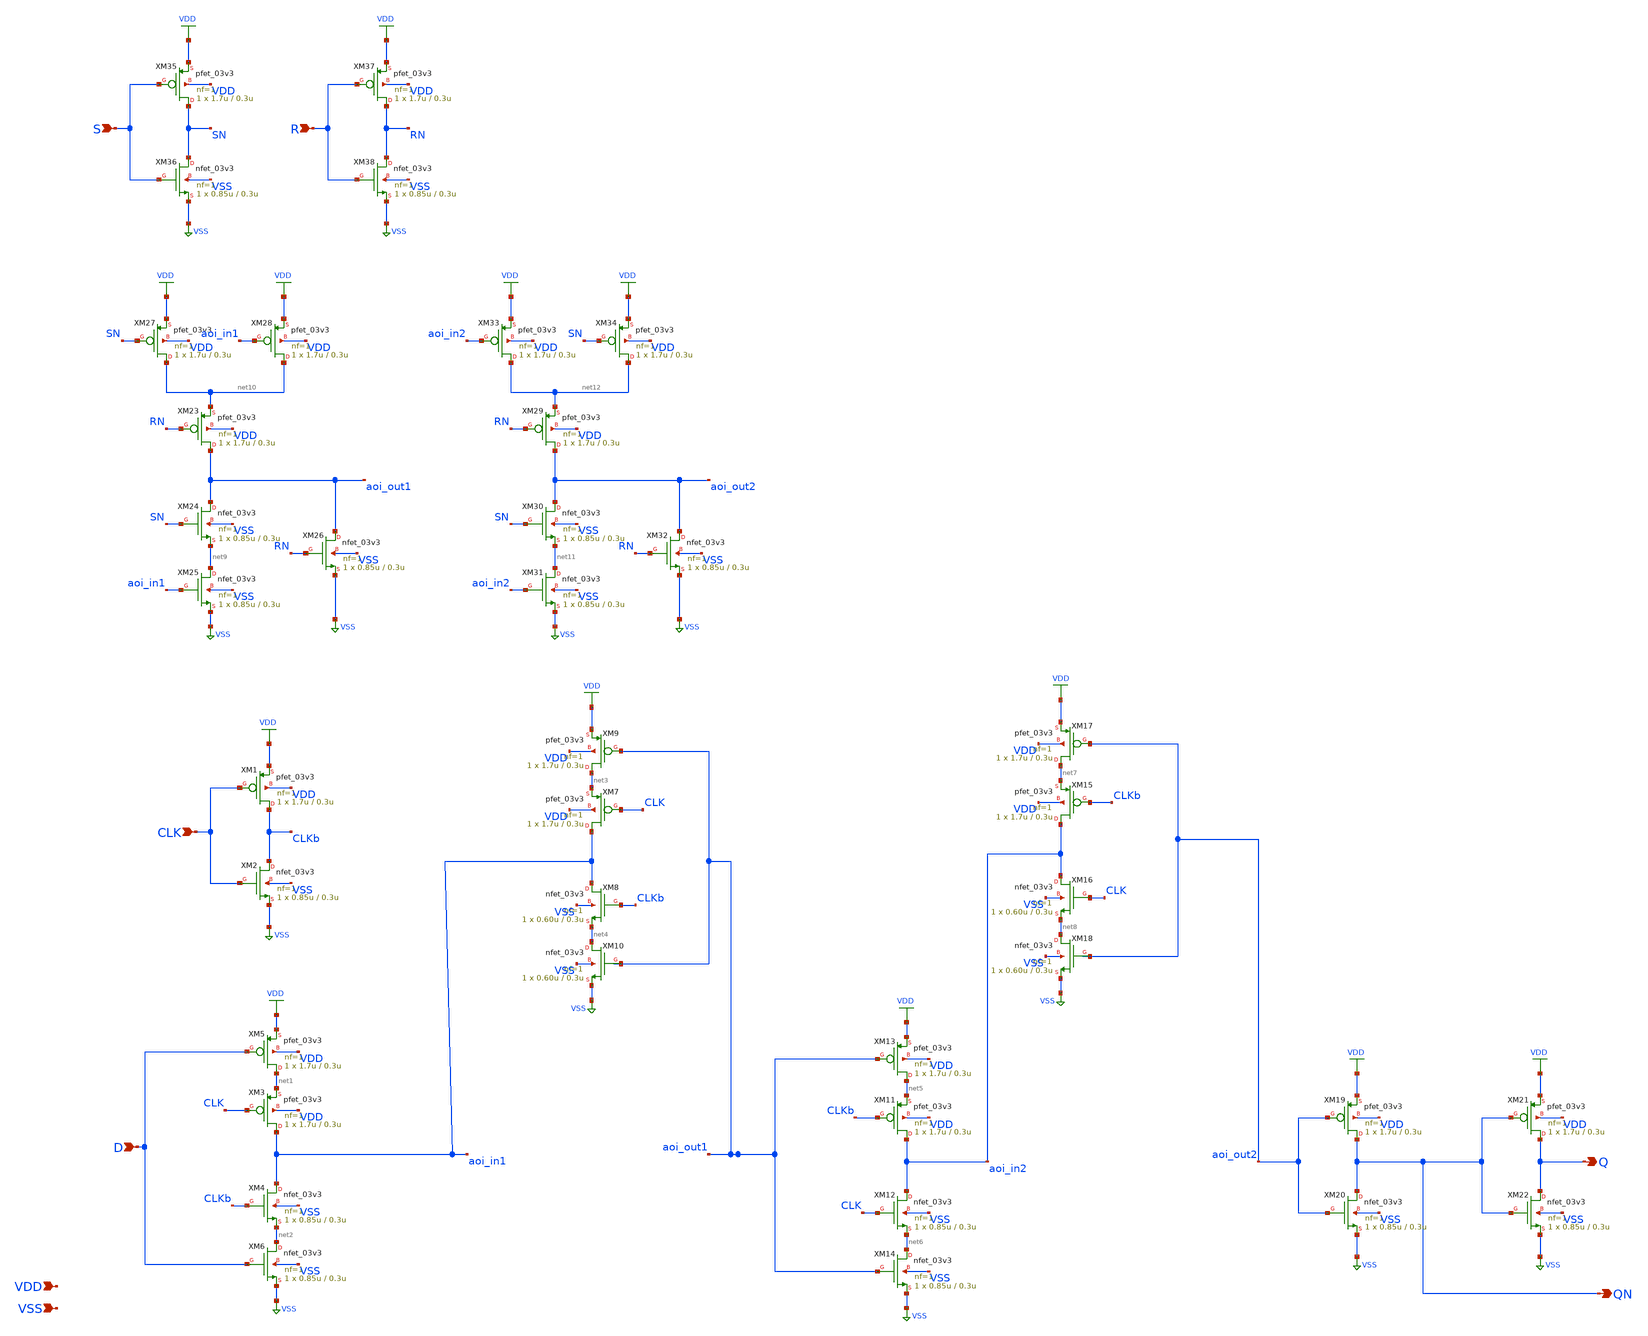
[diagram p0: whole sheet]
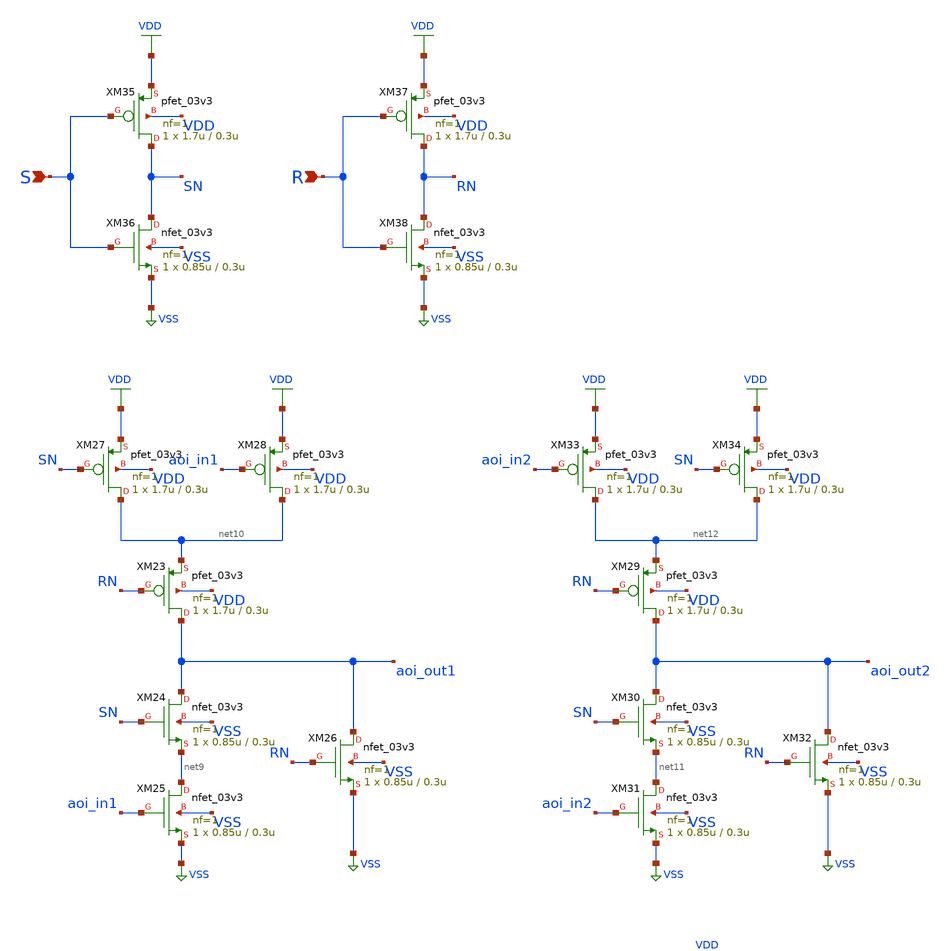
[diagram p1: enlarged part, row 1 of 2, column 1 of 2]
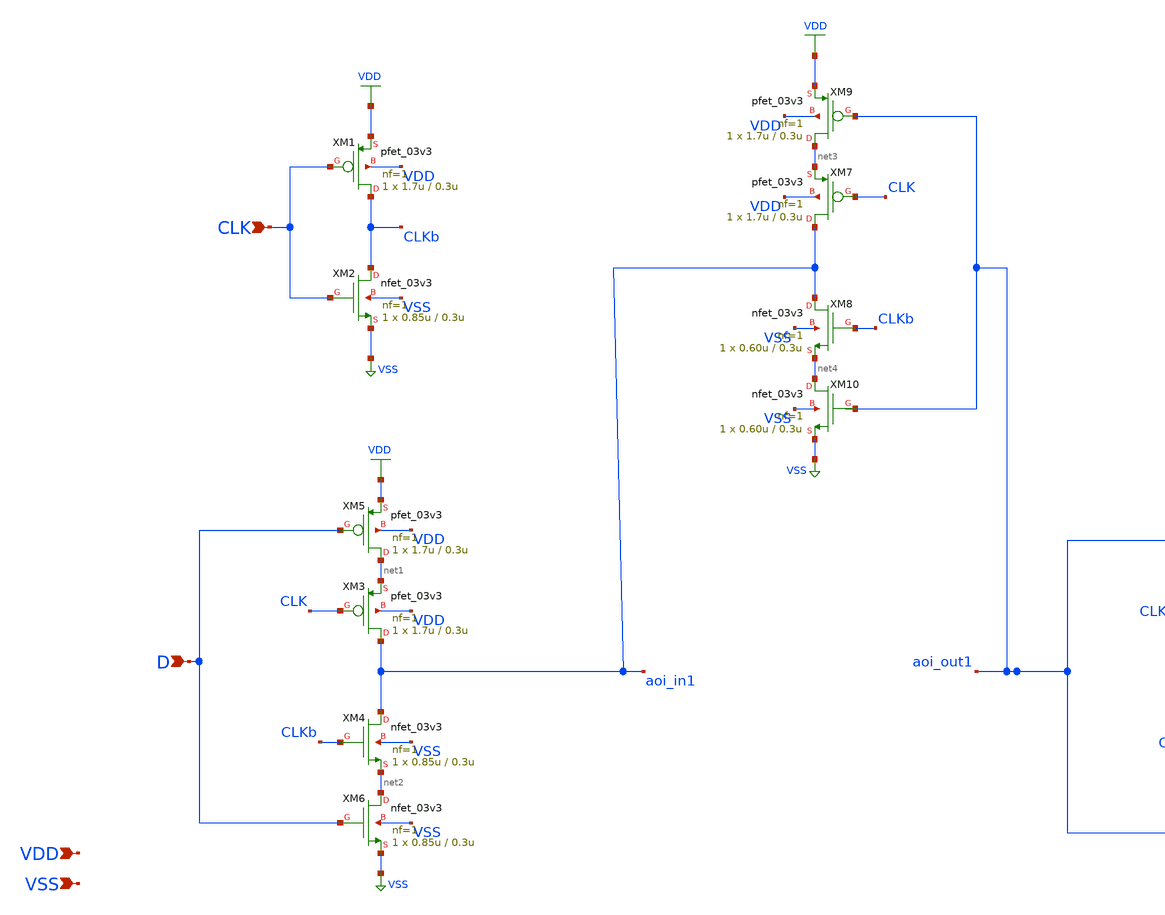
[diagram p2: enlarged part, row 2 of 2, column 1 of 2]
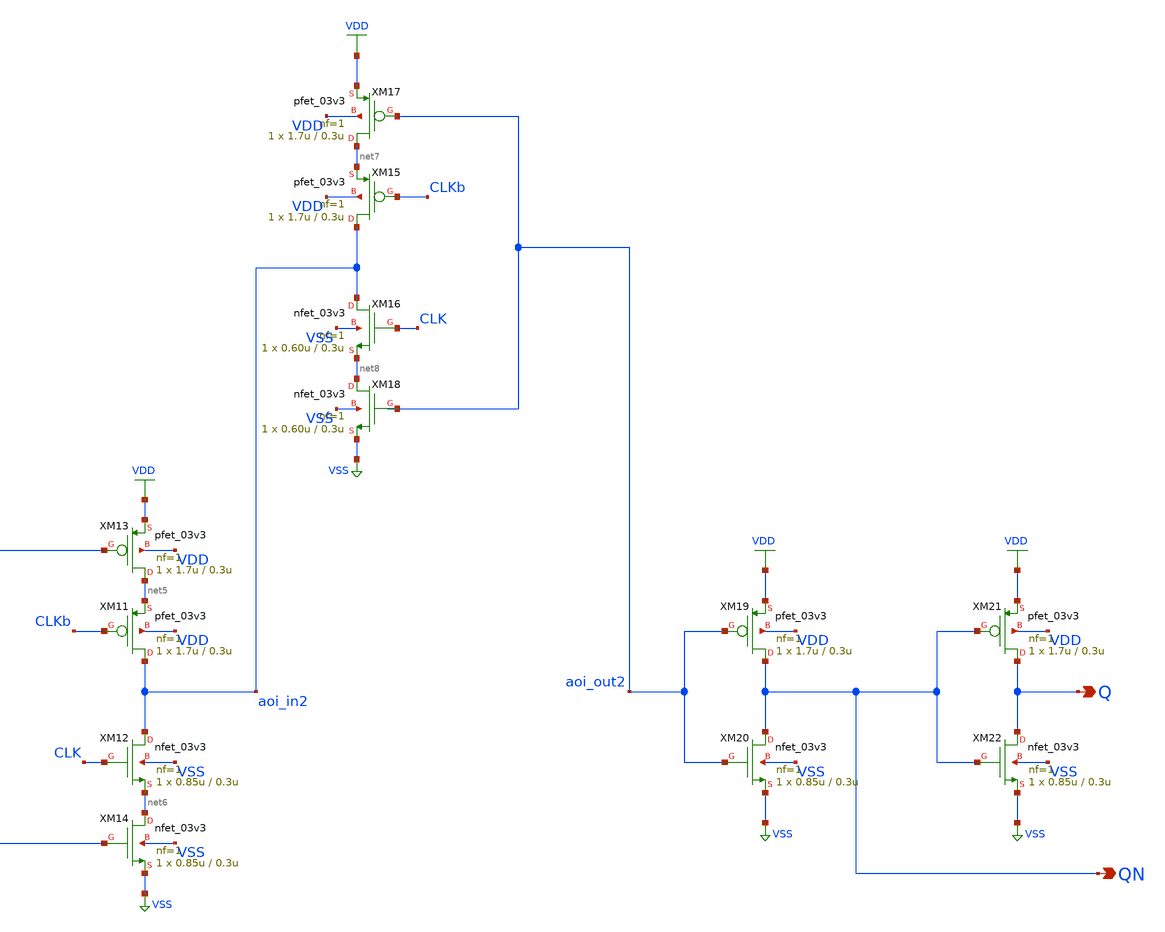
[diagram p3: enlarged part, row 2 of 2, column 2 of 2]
** sch_path: gf180mcu_osu_sc_gp9t3v3/xschem/gf180mcu_osu_sc_gp9t3v3__dffsr_1.sch
**.subckt gf180mcu_osu_sc_gp9t3v3__dffsr_1 D CLK Q QN S R VDD VSS
*.ipin D
*.ipin CLK
*.opin Q
*.opin QN
*.ipin S
*.ipin R
*.ipin VDD
*.ipin VSS
XM1 CLKb CLK VDD VDD pfet_03v3 L=0.3u W=1.7u nf=1 ad='int((nf+1)/2) * W/nf * 0.18u' as='int((nf+2)/2) * W/nf * 0.18u'
+ pd='2*int((nf+1)/2) * (W/nf + 0.18u)' ps='2*int((nf+2)/2) * (W/nf + 0.18u)' nrd='0.18u / W' nrs='0.18u / W'
+ sa=0 sb=0 sd=0 m=1
XM2 CLKb CLK VSS VSS nfet_03v3 L=0.3u W=0.85u nf=1 ad='int((nf+1)/2) * W/nf * 0.18u' as='int((nf+2)/2) * W/nf * 0.18u'
+ pd='2*int((nf+1)/2) * (W/nf + 0.18u)' ps='2*int((nf+2)/2) * (W/nf + 0.18u)' nrd='0.18u / W' nrs='0.18u / W'
+ sa=0 sb=0 sd=0 m=1
XM3 aoi_in1 CLK net1 VDD pfet_03v3 L=0.3u W=1.7u nf=1 ad='int((nf+1)/2) * W/nf * 0.18u' as='int((nf+2)/2) * W/nf * 0.18u'
+ pd='2*int((nf+1)/2) * (W/nf + 0.18u)' ps='2*int((nf+2)/2) * (W/nf + 0.18u)' nrd='0.18u / W' nrs='0.18u / W'
+ sa=0 sb=0 sd=0 m=1
XM4 aoi_in1 CLKb net2 VSS nfet_03v3 L=0.3u W=0.85u nf=1 ad='int((nf+1)/2) * W/nf * 0.18u' as='int((nf+2)/2) * W/nf * 0.18u'
+ pd='2*int((nf+1)/2) * (W/nf + 0.18u)' ps='2*int((nf+2)/2) * (W/nf + 0.18u)' nrd='0.18u / W' nrs='0.18u / W'
+ sa=0 sb=0 sd=0 m=1
XM5 net1 D VDD VDD pfet_03v3 L=0.3u W=1.7u nf=1 ad='int((nf+1)/2) * W/nf * 0.18u' as='int((nf+2)/2) * W/nf * 0.18u'
+ pd='2*int((nf+1)/2) * (W/nf + 0.18u)' ps='2*int((nf+2)/2) * (W/nf + 0.18u)' nrd='0.18u / W' nrs='0.18u / W'
+ sa=0 sb=0 sd=0 m=1
XM6 net2 D VSS VSS nfet_03v3 L=0.3u W=0.85u nf=1 ad='int((nf+1)/2) * W/nf * 0.18u' as='int((nf+2)/2) * W/nf * 0.18u'
+ pd='2*int((nf+1)/2) * (W/nf + 0.18u)' ps='2*int((nf+2)/2) * (W/nf + 0.18u)' nrd='0.18u / W' nrs='0.18u / W'
+ sa=0 sb=0 sd=0 m=1
XM7 aoi_in1 CLK net3 VDD pfet_03v3 L=0.3u W=1.7u nf=1 ad='int((nf+1)/2) * W/nf * 0.18u' as='int((nf+2)/2) * W/nf * 0.18u'
+ pd='2*int((nf+1)/2) * (W/nf + 0.18u)' ps='2*int((nf+2)/2) * (W/nf + 0.18u)' nrd='0.18u / W' nrs='0.18u / W'
+ sa=0 sb=0 sd=0 m=1
XM8 aoi_in1 CLKb net4 VSS nfet_03v3 L=0.3u W=0.60u nf=1 ad='int((nf+1)/2) * W/nf * 0.18u' as='int((nf+2)/2) * W/nf * 0.18u'
+ pd='2*int((nf+1)/2) * (W/nf + 0.18u)' ps='2*int((nf+2)/2) * (W/nf + 0.18u)' nrd='0.18u / W' nrs='0.18u / W'
+ sa=0 sb=0 sd=0 m=1
XM9 net3 aoi_out1 VDD VDD pfet_03v3 L=0.3u W=1.7u nf=1 ad='int((nf+1)/2) * W/nf * 0.18u' as='int((nf+2)/2) * W/nf * 0.18u'
+ pd='2*int((nf+1)/2) * (W/nf + 0.18u)' ps='2*int((nf+2)/2) * (W/nf + 0.18u)' nrd='0.18u / W' nrs='0.18u / W'
+ sa=0 sb=0 sd=0 m=1
XM10 net4 aoi_out1 VSS VSS nfet_03v3 L=0.3u W=0.60u nf=1 ad='int((nf+1)/2) * W/nf * 0.18u' as='int((nf+2)/2) * W/nf * 0.18u'
+ pd='2*int((nf+1)/2) * (W/nf + 0.18u)' ps='2*int((nf+2)/2) * (W/nf + 0.18u)' nrd='0.18u / W' nrs='0.18u / W'
+ sa=0 sb=0 sd=0 m=1
XM11 aoi_in2 CLKb net5 VDD pfet_03v3 L=0.3u W=1.7u nf=1 ad='int((nf+1)/2) * W/nf * 0.18u' as='int((nf+2)/2) * W/nf * 0.18u'
+ pd='2*int((nf+1)/2) * (W/nf + 0.18u)' ps='2*int((nf+2)/2) * (W/nf + 0.18u)' nrd='0.18u / W' nrs='0.18u / W'
+ sa=0 sb=0 sd=0 m=1
XM12 aoi_in2 CLK net6 VSS nfet_03v3 L=0.3u W=0.85u nf=1 ad='int((nf+1)/2) * W/nf * 0.18u' as='int((nf+2)/2) * W/nf * 0.18u'
+ pd='2*int((nf+1)/2) * (W/nf + 0.18u)' ps='2*int((nf+2)/2) * (W/nf + 0.18u)' nrd='0.18u / W' nrs='0.18u / W'
+ sa=0 sb=0 sd=0 m=1
XM13 net5 aoi_out1 VDD VDD pfet_03v3 L=0.3u W=1.7u nf=1 ad='int((nf+1)/2) * W/nf * 0.18u' as='int((nf+2)/2) * W/nf * 0.18u'
+ pd='2*int((nf+1)/2) * (W/nf + 0.18u)' ps='2*int((nf+2)/2) * (W/nf + 0.18u)' nrd='0.18u / W' nrs='0.18u / W'
+ sa=0 sb=0 sd=0 m=1
XM14 net6 aoi_out1 VSS VSS nfet_03v3 L=0.3u W=0.85u nf=1 ad='int((nf+1)/2) * W/nf * 0.18u' as='int((nf+2)/2) * W/nf * 0.18u'
+ pd='2*int((nf+1)/2) * (W/nf + 0.18u)' ps='2*int((nf+2)/2) * (W/nf + 0.18u)' nrd='0.18u / W' nrs='0.18u / W'
+ sa=0 sb=0 sd=0 m=1
XM15 aoi_in2 CLKb net7 VDD pfet_03v3 L=0.3u W=1.7u nf=1 ad='int((nf+1)/2) * W/nf * 0.18u' as='int((nf+2)/2) * W/nf * 0.18u'
+ pd='2*int((nf+1)/2) * (W/nf + 0.18u)' ps='2*int((nf+2)/2) * (W/nf + 0.18u)' nrd='0.18u / W' nrs='0.18u / W'
+ sa=0 sb=0 sd=0 m=1
XM16 aoi_in2 CLK net8 VSS nfet_03v3 L=0.3u W=0.60u nf=1 ad='int((nf+1)/2) * W/nf * 0.18u' as='int((nf+2)/2) * W/nf * 0.18u'
+ pd='2*int((nf+1)/2) * (W/nf + 0.18u)' ps='2*int((nf+2)/2) * (W/nf + 0.18u)' nrd='0.18u / W' nrs='0.18u / W'
+ sa=0 sb=0 sd=0 m=1
XM17 net7 aoi_out2 VDD VDD pfet_03v3 L=0.3u W=1.7u nf=1 ad='int((nf+1)/2) * W/nf * 0.18u' as='int((nf+2)/2) * W/nf * 0.18u'
+ pd='2*int((nf+1)/2) * (W/nf + 0.18u)' ps='2*int((nf+2)/2) * (W/nf + 0.18u)' nrd='0.18u / W' nrs='0.18u / W'
+ sa=0 sb=0 sd=0 m=1
XM18 net8 aoi_out2 VSS VSS nfet_03v3 L=0.3u W=0.60u nf=1 ad='int((nf+1)/2) * W/nf * 0.18u' as='int((nf+2)/2) * W/nf * 0.18u'
+ pd='2*int((nf+1)/2) * (W/nf + 0.18u)' ps='2*int((nf+2)/2) * (W/nf + 0.18u)' nrd='0.18u / W' nrs='0.18u / W'
+ sa=0 sb=0 sd=0 m=1
XM19 QN aoi_out2 VDD VDD pfet_03v3 L=0.3u W=1.7u nf=1 ad='int((nf+1)/2) * W/nf * 0.18u' as='int((nf+2)/2) * W/nf * 0.18u'
+ pd='2*int((nf+1)/2) * (W/nf + 0.18u)' ps='2*int((nf+2)/2) * (W/nf + 0.18u)' nrd='0.18u / W' nrs='0.18u / W'
+ sa=0 sb=0 sd=0 m=1
XM20 QN aoi_out2 VSS VSS nfet_03v3 L=0.3u W=0.85u nf=1 ad='int((nf+1)/2) * W/nf * 0.18u' as='int((nf+2)/2) * W/nf * 0.18u'
+ pd='2*int((nf+1)/2) * (W/nf + 0.18u)' ps='2*int((nf+2)/2) * (W/nf + 0.18u)' nrd='0.18u / W' nrs='0.18u / W'
+ sa=0 sb=0 sd=0 m=1
XM21 Q QN VDD VDD pfet_03v3 L=0.3u W=1.7u nf=1 ad='int((nf+1)/2) * W/nf * 0.18u' as='int((nf+2)/2) * W/nf * 0.18u'
+ pd='2*int((nf+1)/2) * (W/nf + 0.18u)' ps='2*int((nf+2)/2) * (W/nf + 0.18u)' nrd='0.18u / W' nrs='0.18u / W'
+ sa=0 sb=0 sd=0 m=1
XM22 Q QN VSS VSS nfet_03v3 L=0.3u W=0.85u nf=1 ad='int((nf+1)/2) * W/nf * 0.18u' as='int((nf+2)/2) * W/nf * 0.18u'
+ pd='2*int((nf+1)/2) * (W/nf + 0.18u)' ps='2*int((nf+2)/2) * (W/nf + 0.18u)' nrd='0.18u / W' nrs='0.18u / W'
+ sa=0 sb=0 sd=0 m=1
XM23 aoi_out1 RN net10 VDD pfet_03v3 L=0.3u W=1.7u nf=1 ad='int((nf+1)/2) * W/nf * 0.18u' as='int((nf+2)/2) * W/nf * 0.18u'
+ pd='2*int((nf+1)/2) * (W/nf + 0.18u)' ps='2*int((nf+2)/2) * (W/nf + 0.18u)' nrd='0.18u / W' nrs='0.18u / W'
+ sa=0 sb=0 sd=0 m=1
XM24 aoi_out1 SN net9 VSS nfet_03v3 L=0.3u W=0.85u nf=1 ad='int((nf+1)/2) * W/nf * 0.18u' as='int((nf+2)/2) * W/nf * 0.18u'
+ pd='2*int((nf+1)/2) * (W/nf + 0.18u)' ps='2*int((nf+2)/2) * (W/nf + 0.18u)' nrd='0.18u / W' nrs='0.18u / W'
+ sa=0 sb=0 sd=0 m=1
XM25 net9 aoi_in1 VSS VSS nfet_03v3 L=0.3u W=0.85u nf=1 ad='int((nf+1)/2) * W/nf * 0.18u' as='int((nf+2)/2) * W/nf * 0.18u'
+ pd='2*int((nf+1)/2) * (W/nf + 0.18u)' ps='2*int((nf+2)/2) * (W/nf + 0.18u)' nrd='0.18u / W' nrs='0.18u / W'
+ sa=0 sb=0 sd=0 m=1
XM26 aoi_out1 RN VSS VSS nfet_03v3 L=0.3u W=0.85u nf=1 ad='int((nf+1)/2) * W/nf * 0.18u' as='int((nf+2)/2) * W/nf * 0.18u'
+ pd='2*int((nf+1)/2) * (W/nf + 0.18u)' ps='2*int((nf+2)/2) * (W/nf + 0.18u)' nrd='0.18u / W' nrs='0.18u / W'
+ sa=0 sb=0 sd=0 m=1
XM27 net10 SN VDD VDD pfet_03v3 L=0.3u W=1.7u nf=1 ad='int((nf+1)/2) * W/nf * 0.18u' as='int((nf+2)/2) * W/nf * 0.18u'
+ pd='2*int((nf+1)/2) * (W/nf + 0.18u)' ps='2*int((nf+2)/2) * (W/nf + 0.18u)' nrd='0.18u / W' nrs='0.18u / W'
+ sa=0 sb=0 sd=0 m=1
XM28 net10 aoi_in1 VDD VDD pfet_03v3 L=0.3u W=1.7u nf=1 ad='int((nf+1)/2) * W/nf * 0.18u' as='int((nf+2)/2) * W/nf * 0.18u'
+ pd='2*int((nf+1)/2) * (W/nf + 0.18u)' ps='2*int((nf+2)/2) * (W/nf + 0.18u)' nrd='0.18u / W' nrs='0.18u / W'
+ sa=0 sb=0 sd=0 m=1
XM29 aoi_out2 RN net12 VDD pfet_03v3 L=0.3u W=1.7u nf=1 ad='int((nf+1)/2) * W/nf * 0.18u' as='int((nf+2)/2) * W/nf * 0.18u'
+ pd='2*int((nf+1)/2) * (W/nf + 0.18u)' ps='2*int((nf+2)/2) * (W/nf + 0.18u)' nrd='0.18u / W' nrs='0.18u / W'
+ sa=0 sb=0 sd=0 m=1
XM30 aoi_out2 SN net11 VSS nfet_03v3 L=0.3u W=0.85u nf=1 ad='int((nf+1)/2) * W/nf * 0.18u' as='int((nf+2)/2) * W/nf * 0.18u'
+ pd='2*int((nf+1)/2) * (W/nf + 0.18u)' ps='2*int((nf+2)/2) * (W/nf + 0.18u)' nrd='0.18u / W' nrs='0.18u / W'
+ sa=0 sb=0 sd=0 m=1
XM31 net11 aoi_in2 VSS VSS nfet_03v3 L=0.3u W=0.85u nf=1 ad='int((nf+1)/2) * W/nf * 0.18u' as='int((nf+2)/2) * W/nf * 0.18u'
+ pd='2*int((nf+1)/2) * (W/nf + 0.18u)' ps='2*int((nf+2)/2) * (W/nf + 0.18u)' nrd='0.18u / W' nrs='0.18u / W'
+ sa=0 sb=0 sd=0 m=1
XM32 aoi_out2 RN VSS VSS nfet_03v3 L=0.3u W=0.85u nf=1 ad='int((nf+1)/2) * W/nf * 0.18u' as='int((nf+2)/2) * W/nf * 0.18u'
+ pd='2*int((nf+1)/2) * (W/nf + 0.18u)' ps='2*int((nf+2)/2) * (W/nf + 0.18u)' nrd='0.18u / W' nrs='0.18u / W'
+ sa=0 sb=0 sd=0 m=1
XM33 net12 aoi_in2 VDD VDD pfet_03v3 L=0.3u W=1.7u nf=1 ad='int((nf+1)/2) * W/nf * 0.18u' as='int((nf+2)/2) * W/nf * 0.18u'
+ pd='2*int((nf+1)/2) * (W/nf + 0.18u)' ps='2*int((nf+2)/2) * (W/nf + 0.18u)' nrd='0.18u / W' nrs='0.18u / W'
+ sa=0 sb=0 sd=0 m=1
XM34 net12 SN VDD VDD pfet_03v3 L=0.3u W=1.7u nf=1 ad='int((nf+1)/2) * W/nf * 0.18u' as='int((nf+2)/2) * W/nf * 0.18u'
+ pd='2*int((nf+1)/2) * (W/nf + 0.18u)' ps='2*int((nf+2)/2) * (W/nf + 0.18u)' nrd='0.18u / W' nrs='0.18u / W'
+ sa=0 sb=0 sd=0 m=1
XM35 SN S VDD VDD pfet_03v3 L=0.3u W=1.7u nf=1 ad='int((nf+1)/2) * W/nf * 0.18u' as='int((nf+2)/2) * W/nf * 0.18u'
+ pd='2*int((nf+1)/2) * (W/nf + 0.18u)' ps='2*int((nf+2)/2) * (W/nf + 0.18u)' nrd='0.18u / W' nrs='0.18u / W'
+ sa=0 sb=0 sd=0 m=1
XM36 SN S VSS VSS nfet_03v3 L=0.3u W=0.85u nf=1 ad='int((nf+1)/2) * W/nf * 0.18u' as='int((nf+2)/2) * W/nf * 0.18u'
+ pd='2*int((nf+1)/2) * (W/nf + 0.18u)' ps='2*int((nf+2)/2) * (W/nf + 0.18u)' nrd='0.18u / W' nrs='0.18u / W'
+ sa=0 sb=0 sd=0 m=1
XM37 RN R VDD VDD pfet_03v3 L=0.3u W=1.7u nf=1 ad='int((nf+1)/2) * W/nf * 0.18u' as='int((nf+2)/2) * W/nf * 0.18u'
+ pd='2*int((nf+1)/2) * (W/nf + 0.18u)' ps='2*int((nf+2)/2) * (W/nf + 0.18u)' nrd='0.18u / W' nrs='0.18u / W'
+ sa=0 sb=0 sd=0 m=1
XM38 RN R VSS VSS nfet_03v3 L=0.3u W=0.85u nf=1 ad='int((nf+1)/2) * W/nf * 0.18u' as='int((nf+2)/2) * W/nf * 0.18u'
+ pd='2*int((nf+1)/2) * (W/nf + 0.18u)' ps='2*int((nf+2)/2) * (W/nf + 0.18u)' nrd='0.18u / W' nrs='0.18u / W'
+ sa=0 sb=0 sd=0 m=1
**.ends
.GLOBAL VDD
.GLOBAL VSS
.end
